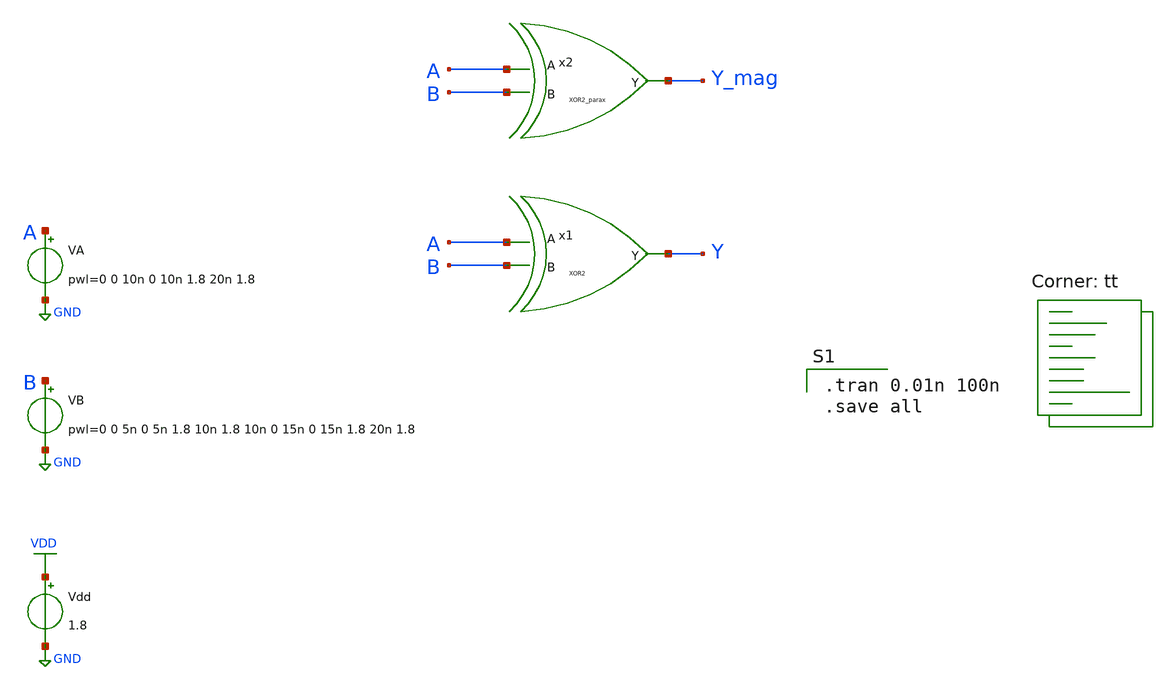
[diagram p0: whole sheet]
** sch_path: xor2sim.sch
**.subckt xor2sim
x1 A B Y XOR2
Vdd VDD GND 1.8
VA A GND pwl=0 0 10n 0 10n 1.8 20n 1.8
VB B GND pwl=0 0 5n 0 5n 1.8 10n 1.8 10n 0 15n 0 15n 1.8 20n 1.8
x2 A B Y_mag XOR2_parax
**** begin user architecture code

.tran 0.01n 100n
.save all

.lib $::SKYWATER_MODELS/sky130.lib.spice tt
**** end user architecture code
**.ends

* expanding   symbol:  gates/XOR2.sym # of pins=3
** sym_path: gates/XOR2.sym
** sch_path: gates/XOR2.sch
.subckt XOR2 B A Y
*.ipin A
*.ipin B
*.opin Y
XM1 Y A net5 GND sky130_fd_pr__nfet_01v8 L=0.15 W=1 nf=1 ad='int((nf+1)/2) * W/nf * 0.29' as='int((nf+2)/2) * W/nf * 0.29'
+ pd='2*int((nf+1)/2) * (W/nf + 0.29)' ps='2*int((nf+2)/2) * (W/nf + 0.29)' nrd='0.29 / W' nrs='0.29 / W'
+ sa=0 sb=0 sd=0 mult=1 m=1
XM2 net5 B GND GND sky130_fd_pr__nfet_01v8 L=0.15 W=1 nf=1 ad='int((nf+1)/2) * W/nf * 0.29' as='int((nf+2)/2) * W/nf * 0.29'
+ pd='2*int((nf+1)/2) * (W/nf + 0.29)' ps='2*int((nf+2)/2) * (W/nf + 0.29)' nrd='0.29 / W' nrs='0.29 / W'
+ sa=0 sb=0 sd=0 mult=1 m=1
XM3 Y net1 net2 VDD sky130_fd_pr__pfet_01v8 L=0.15 W=1 nf=1 ad='int((nf+1)/2) * W/nf * 0.29' as='int((nf+2)/2) * W/nf * 0.29'
+ pd='2*int((nf+1)/2) * (W/nf + 0.29)' ps='2*int((nf+2)/2) * (W/nf + 0.29)' nrd='0.29 / W' nrs='0.29 / W'
+ sa=0 sb=0 sd=0 mult=1 m=1
XM4 net2 A VDD VDD sky130_fd_pr__pfet_01v8 L=0.15 W=1 nf=1 ad='int((nf+1)/2) * W/nf * 0.29' as='int((nf+2)/2) * W/nf * 0.29'
+ pd='2*int((nf+1)/2) * (W/nf + 0.29)' ps='2*int((nf+2)/2) * (W/nf + 0.29)' nrd='0.29 / W' nrs='0.29 / W'
+ sa=0 sb=0 sd=0 mult=1 m=1
XM5 net2 B VDD VDD sky130_fd_pr__pfet_01v8 L=0.15 W=1 nf=1 ad='int((nf+1)/2) * W/nf * 0.29' as='int((nf+2)/2) * W/nf * 0.29'
+ pd='2*int((nf+1)/2) * (W/nf + 0.29)' ps='2*int((nf+2)/2) * (W/nf + 0.29)' nrd='0.29 / W' nrs='0.29 / W'
+ sa=0 sb=0 sd=0 mult=1 m=1
XM6 Y net3 net2 VDD sky130_fd_pr__pfet_01v8 L=0.15 W=1 nf=1 ad='int((nf+1)/2) * W/nf * 0.29' as='int((nf+2)/2) * W/nf * 0.29'
+ pd='2*int((nf+1)/2) * (W/nf + 0.29)' ps='2*int((nf+2)/2) * (W/nf + 0.29)' nrd='0.29 / W' nrs='0.29 / W'
+ sa=0 sb=0 sd=0 mult=1 m=1
XM7 Y net1 net4 GND sky130_fd_pr__nfet_01v8 L=0.15 W=1 nf=1 ad='int((nf+1)/2) * W/nf * 0.29' as='int((nf+2)/2) * W/nf * 0.29'
+ pd='2*int((nf+1)/2) * (W/nf + 0.29)' ps='2*int((nf+2)/2) * (W/nf + 0.29)' nrd='0.29 / W' nrs='0.29 / W'
+ sa=0 sb=0 sd=0 mult=1 m=1
XM8 net4 net3 GND GND sky130_fd_pr__nfet_01v8 L=0.15 W=1 nf=1 ad='int((nf+1)/2) * W/nf * 0.29' as='int((nf+2)/2) * W/nf * 0.29'
+ pd='2*int((nf+1)/2) * (W/nf + 0.29)' ps='2*int((nf+2)/2) * (W/nf + 0.29)' nrd='0.29 / W' nrs='0.29 / W'
+ sa=0 sb=0 sd=0 mult=1 m=1
X1 A net1 inv_vtc
X2 B net3 inv_vtc
.ends


* expanding   symbol:  gates/XOR2_parax.sym # of pins=3
** sym_path: gates/XOR2.sym
.include [file normalize /home/apn/mag_gates/XOR2_parax.spice]

* expanding   symbol:  inv_vtc.sym # of pins=2
** sym_path: inv_vtc.sym
** sch_path: inv_vtc.sch
.subckt inv_vtc A Y
*.ipin A
*.opin Y
XM1 Y A VDD VDD sky130_fd_pr__pfet_01v8 L=0.15 W=2 nf=1 ad='int((nf+1)/2) * W/nf * 0.29' as='int((nf+2)/2) * W/nf * 0.29'
+ pd='2*int((nf+1)/2) * (W/nf + 0.29)' ps='2*int((nf+2)/2) * (W/nf + 0.29)' nrd='0.29 / W' nrs='0.29 / W'
+ sa=0 sb=0 sd=0 mult=1 m=1
XM2 Y A GND GND sky130_fd_pr__nfet_01v8 L=0.15 W=1 nf=1 ad='int((nf+1)/2) * W/nf * 0.29' as='int((nf+2)/2) * W/nf * 0.29'
+ pd='2*int((nf+1)/2) * (W/nf + 0.29)' ps='2*int((nf+2)/2) * (W/nf + 0.29)' nrd='0.29 / W' nrs='0.29 / W'
+ sa=0 sb=0 sd=0 mult=1 m=1
.ends

.GLOBAL VDD
.GLOBAL GND
.end
